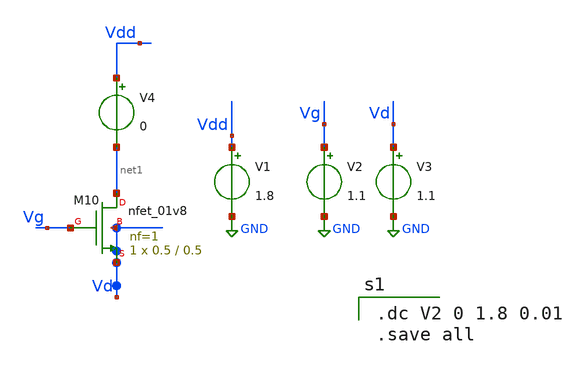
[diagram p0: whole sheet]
** sch_path: xschem/xschemfiles/ntest.sch
**.subckt ntest
V1 Vdd GND 1.8
V2 Vg GND 1.1
V3 Vd GND 1.1
V4 Vdd net1 0
XM10 net1 Vg Vd Vd sky130_fd_pr__nfet_01v8 L=0.5 W=0.5 nf=1 ad='int((nf+1)/2) * W/nf * 0.29' as='int((nf+2)/2) * W/nf * 0.29'
+ pd='2*int((nf+1)/2) * (W/nf + 0.29)' ps='2*int((nf+2)/2) * (W/nf + 0.29)' nrd='0.29 / W' nrs='0.29 / W'
+ sa=0 sb=0 sd=0 mult=1 m=1
**** begin user architecture code

.dc V2 0 1.8 0.01
.save all


** opencircuitdesign pdks install
.lib $::SKYWATER_MODELS/sky130.lib.spice tt


**** end user architecture code
**.ends
.GLOBAL GND
.end
